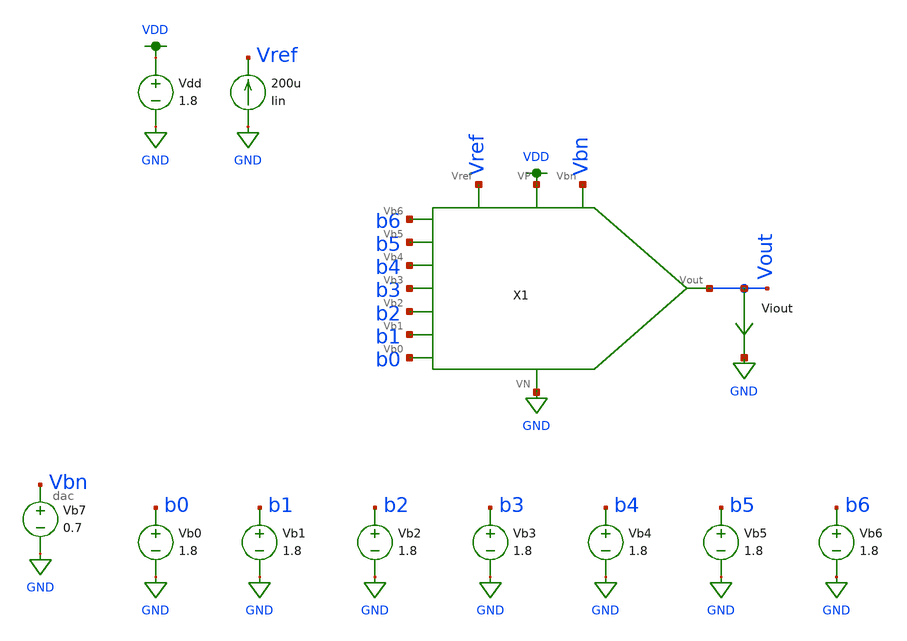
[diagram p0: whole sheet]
** sch_path: dac/schematics/misc/dac_sim.sch
**.subckt dac_sim
Vdd VDD GND 1.8
Viout Vout GND 0
.save i(viout)
Vb0 b0 GND 1.8
Vb1 b1 GND 1.8
Vb2 b2 GND 1.8
Vb3 b3 GND 1.8
Vb4 b4 GND 1.8
Vb5 b5 GND 1.8
Vb6 b6 GND 1.8
Iin GND Vref 200u
X1 b6 b5 b4 b3 b2 b1 b0 Vout VDD GND Vref Vbn dac
Vb7 Vbn GND 0.7
**** begin user architecture code

.option wnflag=1
.param MC_SWITCH=1.0
.lib ~/skywater/skywater-pdk/libraries/sky130_fd_pr_ngspice/latest/models/sky130.lib.spice tt


.control
  set wr_vecnames
  set wr_singlescale
  let code = 0
  while code < 128
    if (code % 2) eq 0
      let b0 = 1.8
    else
      let b0 = 0
    end
    if (floor(code / 2) % 2) eq 0
      let b1 = 1.8
    else
      let b1 = 0
    end
    if (floor(code / 4) % 2) eq 0
      let b2 = 1.8
    else
      let b2 = 0
    end
    if (floor(code / 8) % 2) eq 0
      let b3 = 1.8
    else
      let b3 = 0
    end
    if (floor(code / 16) % 2) eq 0
      let b4 = 1.8
    else
      let b4 = 0
    end
    if (floor(code / 32) % 2) eq 0
      let b5 = 1.8
    else
      let b5 = 0
    end
    if (floor(code / 64) % 2) eq 0
      let b6 = 1.8
    else
      let b6 = 0
    end
    alter vb0 $&b0
    alter vb1 $&b1
    alter vb2 $&b2
    alter vb3 $&b3
    alter vb4 $&b4
    alter vb5 $&b5
    alter vb6 $&b6
    save all
    op
    wrdata ~/current-output-dac-vlsi/simulations/dacsim.txt v(b0) v(b1) v(b2) v(b3) v(b4) v(b5)
+ v(b6) i(Viout) v(Vout)
    if code eq 0
      set appendwrite
      set wr_vecnames = FALSE
    end
    let code = code + 1
  end
  quit
.endc

**** end user architecture code
**.ends

* expanding   symbol:  /home/madvlsi/current-output-dac-vlsi/schematics/dac.sym # of pins=12
** sym_path: dac/schematics/misc/dac.sym
** sch_path: dac/schematics/misc/dac.sch
.subckt dac Vb6 Vb5 Vb4 Vb3 Vb2 Vb1 Vb0 Vout VP VN Vref Vbn
*.iopin VN
*.iopin VP
*.opin Vout
*.ipin Vref
*.ipin Vb6
*.ipin Vb5
*.ipin Vb4
*.ipin Vb3
*.ipin Vb2
*.ipin Vb1
*.ipin Vb0
*.iopin Vbn
XM1 VN Vref Vref GND sky130_fd_pr__nfet_01v8 L=0.5 W=1 nf=1 ad='int((nf+1)/2) * W/nf * 0.29' as='int((nf+2)/2) * W/nf * 0.29'
+ pd='2*int((nf+1)/2) * (W/nf + 0.29)' ps='2*int((nf+2)/2) * (W/nf + 0.29)' nrd='0.29 / W' nrs='0.29 / W'
+ sa=0 sb=0 sd=0 mult=1 m=1
XM3 net2 Vref net1 GND sky130_fd_pr__nfet_01v8 L=0.5 W=1 nf=1 ad='int((nf+1)/2) * W/nf * 0.29' as='int((nf+2)/2) * W/nf * 0.29'
+ pd='2*int((nf+1)/2) * (W/nf + 0.29)' ps='2*int((nf+2)/2) * (W/nf + 0.29)' nrd='0.29 / W' nrs='0.29 / W'
+ sa=0 sb=0 sd=0 mult=2 m=2
XM2 VP Vref net1 GND sky130_fd_pr__nfet_01v8 L=0.5 W=1 nf=1 ad='int((nf+1)/2) * W/nf * 0.29' as='int((nf+2)/2) * W/nf * 0.29'
+ pd='2*int((nf+1)/2) * (W/nf + 0.29)' ps='2*int((nf+2)/2) * (W/nf + 0.29)' nrd='0.29 / W' nrs='0.29 / W'
+ sa=0 sb=0 sd=0 mult=1 m=1
XM4 VP Vref net2 GND sky130_fd_pr__nfet_01v8 L=0.5 W=1 nf=1 ad='int((nf+1)/2) * W/nf * 0.29' as='int((nf+2)/2) * W/nf * 0.29'
+ pd='2*int((nf+1)/2) * (W/nf + 0.29)' ps='2*int((nf+2)/2) * (W/nf + 0.29)' nrd='0.29 / W' nrs='0.29 / W'
+ sa=0 sb=0 sd=0 mult=1 m=1
XM6 VP Vref net3 GND sky130_fd_pr__nfet_01v8 L=0.5 W=1 nf=1 ad='int((nf+1)/2) * W/nf * 0.29' as='int((nf+2)/2) * W/nf * 0.29'
+ pd='2*int((nf+1)/2) * (W/nf + 0.29)' ps='2*int((nf+2)/2) * (W/nf + 0.29)' nrd='0.29 / W' nrs='0.29 / W'
+ sa=0 sb=0 sd=0 mult=1 m=1
XM8 VP Vref net4 GND sky130_fd_pr__nfet_01v8 L=0.5 W=1 nf=1 ad='int((nf+1)/2) * W/nf * 0.29' as='int((nf+2)/2) * W/nf * 0.29'
+ pd='2*int((nf+1)/2) * (W/nf + 0.29)' ps='2*int((nf+2)/2) * (W/nf + 0.29)' nrd='0.29 / W' nrs='0.29 / W'
+ sa=0 sb=0 sd=0 mult=1 m=1
XM10 VP Vref net5 GND sky130_fd_pr__nfet_01v8 L=0.5 W=1 nf=1 ad='int((nf+1)/2) * W/nf * 0.29' as='int((nf+2)/2) * W/nf * 0.29'
+ pd='2*int((nf+1)/2) * (W/nf + 0.29)' ps='2*int((nf+2)/2) * (W/nf + 0.29)' nrd='0.29 / W' nrs='0.29 / W'
+ sa=0 sb=0 sd=0 mult=1 m=1
XM12 VP Vref net6 GND sky130_fd_pr__nfet_01v8 L=0.5 W=1 nf=1 ad='int((nf+1)/2) * W/nf * 0.29' as='int((nf+2)/2) * W/nf * 0.29'
+ pd='2*int((nf+1)/2) * (W/nf + 0.29)' ps='2*int((nf+2)/2) * (W/nf + 0.29)' nrd='0.29 / W' nrs='0.29 / W'
+ sa=0 sb=0 sd=0 mult=1 m=1
XM14 Vout Vref net7 GND sky130_fd_pr__nfet_01v8 L=0.5 W=1 nf=1 ad='int((nf+1)/2) * W/nf * 0.29' as='int((nf+2)/2) * W/nf * 0.29'
+ pd='2*int((nf+1)/2) * (W/nf + 0.29)' ps='2*int((nf+2)/2) * (W/nf + 0.29)' nrd='0.29 / W' nrs='0.29 / W'
+ sa=0 sb=0 sd=0 mult=2 m=2
XM5 net3 Vref net2 GND sky130_fd_pr__nfet_01v8 L=0.5 W=1 nf=1 ad='int((nf+1)/2) * W/nf * 0.29' as='int((nf+2)/2) * W/nf * 0.29'
+ pd='2*int((nf+1)/2) * (W/nf + 0.29)' ps='2*int((nf+2)/2) * (W/nf + 0.29)' nrd='0.29 / W' nrs='0.29 / W'
+ sa=0 sb=0 sd=0 mult=2 m=2
XM7 net4 Vref net3 GND sky130_fd_pr__nfet_01v8 L=0.5 W=1 nf=1 ad='int((nf+1)/2) * W/nf * 0.29' as='int((nf+2)/2) * W/nf * 0.29'
+ pd='2*int((nf+1)/2) * (W/nf + 0.29)' ps='2*int((nf+2)/2) * (W/nf + 0.29)' nrd='0.29 / W' nrs='0.29 / W'
+ sa=0 sb=0 sd=0 mult=2 m=2
XM9 net5 Vref net4 GND sky130_fd_pr__nfet_01v8 L=0.5 W=1 nf=1 ad='int((nf+1)/2) * W/nf * 0.29' as='int((nf+2)/2) * W/nf * 0.29'
+ pd='2*int((nf+1)/2) * (W/nf + 0.29)' ps='2*int((nf+2)/2) * (W/nf + 0.29)' nrd='0.29 / W' nrs='0.29 / W'
+ sa=0 sb=0 sd=0 mult=2 m=2
XM11 net6 Vref net5 GND sky130_fd_pr__nfet_01v8 L=0.5 W=1 nf=1 ad='int((nf+1)/2) * W/nf * 0.29' as='int((nf+2)/2) * W/nf * 0.29'
+ pd='2*int((nf+1)/2) * (W/nf + 0.29)' ps='2*int((nf+2)/2) * (W/nf + 0.29)' nrd='0.29 / W' nrs='0.29 / W'
+ sa=0 sb=0 sd=0 mult=2 m=2
XM13 net7 Vref net6 GND sky130_fd_pr__nfet_01v8 L=0.5 W=1 nf=1 ad='int((nf+1)/2) * W/nf * 0.29' as='int((nf+2)/2) * W/nf * 0.29'
+ pd='2*int((nf+1)/2) * (W/nf + 0.29)' ps='2*int((nf+2)/2) * (W/nf + 0.29)' nrd='0.29 / W' nrs='0.29 / W'
+ sa=0 sb=0 sd=0 mult=2 m=2
XM16 net2 net8 VN GND sky130_fd_pr__nfet_01v8 L=0.5 W=1 nf=1 ad='int((nf+1)/2) * W/nf * 0.29' as='int((nf+2)/2) * W/nf * 0.29'
+ pd='2*int((nf+1)/2) * (W/nf + 0.29)' ps='2*int((nf+2)/2) * (W/nf + 0.29)' nrd='0.29 / W' nrs='0.29 / W'
+ sa=0 sb=0 sd=0 mult=1 m=1
XM17 net1 net9 VN GND sky130_fd_pr__nfet_01v8 L=0.5 W=1 nf=1 ad='int((nf+1)/2) * W/nf * 0.29' as='int((nf+2)/2) * W/nf * 0.29'
+ pd='2*int((nf+1)/2) * (W/nf + 0.29)' ps='2*int((nf+2)/2) * (W/nf + 0.29)' nrd='0.29 / W' nrs='0.29 / W'
+ sa=0 sb=0 sd=0 mult=1 m=1
XM18 net3 net11 VN GND sky130_fd_pr__nfet_01v8 L=0.5 W=1 nf=1 ad='int((nf+1)/2) * W/nf * 0.29' as='int((nf+2)/2) * W/nf * 0.29'
+ pd='2*int((nf+1)/2) * (W/nf + 0.29)' ps='2*int((nf+2)/2) * (W/nf + 0.29)' nrd='0.29 / W' nrs='0.29 / W'
+ sa=0 sb=0 sd=0 mult=1 m=1
XM19 net4 net10 VN GND sky130_fd_pr__nfet_01v8 L=0.5 W=1 nf=1 ad='int((nf+1)/2) * W/nf * 0.29' as='int((nf+2)/2) * W/nf * 0.29'
+ pd='2*int((nf+1)/2) * (W/nf + 0.29)' ps='2*int((nf+2)/2) * (W/nf + 0.29)' nrd='0.29 / W' nrs='0.29 / W'
+ sa=0 sb=0 sd=0 mult=1 m=1
XM20 net5 net14 VN GND sky130_fd_pr__nfet_01v8 L=0.5 W=1 nf=1 ad='int((nf+1)/2) * W/nf * 0.29' as='int((nf+2)/2) * W/nf * 0.29'
+ pd='2*int((nf+1)/2) * (W/nf + 0.29)' ps='2*int((nf+2)/2) * (W/nf + 0.29)' nrd='0.29 / W' nrs='0.29 / W'
+ sa=0 sb=0 sd=0 mult=1 m=1
XM21 net6 net13 VN GND sky130_fd_pr__nfet_01v8 L=0.5 W=1 nf=1 ad='int((nf+1)/2) * W/nf * 0.29' as='int((nf+2)/2) * W/nf * 0.29'
+ pd='2*int((nf+1)/2) * (W/nf + 0.29)' ps='2*int((nf+2)/2) * (W/nf + 0.29)' nrd='0.29 / W' nrs='0.29 / W'
+ sa=0 sb=0 sd=0 mult=1 m=1
XM22 net7 net12 VN GND sky130_fd_pr__nfet_01v8 L=0.5 W=1 nf=1 ad='int((nf+1)/2) * W/nf * 0.29' as='int((nf+2)/2) * W/nf * 0.29'
+ pd='2*int((nf+1)/2) * (W/nf + 0.29)' ps='2*int((nf+2)/2) * (W/nf + 0.29)' nrd='0.29 / W' nrs='0.29 / W'
+ sa=0 sb=0 sd=0 mult=1 m=1
X1 Vbn VN net9 Vb6 mux
X2 Vbn VN net8 Vb5 mux
X3 Vbn VN net11 Vb4 mux
X4 Vbn VN net10 Vb3 mux
X5 Vbn VN net14 Vb2 mux
X6 Vbn VN net13 Vb1 mux
X7 Vbn VN net12 Vb0 mux
.ends


* expanding   symbol:  /home/madvlsi/current-output-dac-vlsi/schematics/mux.sym # of pins=4
** sym_path: dac/schematics/mux.sym
** sch_path: dac/schematics/mux.sch
.subckt mux A B Y S
*.ipin A
*.ipin B
*.ipin S
*.opin Y
XM1 A S Y VDD sky130_fd_pr__pfet_01v8 L=0.15 W=1 nf=1 ad='int((nf+1)/2) * W/nf * 0.29' as='int((nf+2)/2) * W/nf * 0.29'
+ pd='2*int((nf+1)/2) * (W/nf + 0.29)' ps='2*int((nf+2)/2) * (W/nf + 0.29)' nrd='0.29 / W' nrs='0.29 / W'
+ sa=0 sb=0 sd=0 mult=1 m=1
XM3 net1 S VDD VDD sky130_fd_pr__pfet_01v8 L=0.15 W=1 nf=1 ad='int((nf+1)/2) * W/nf * 0.29' as='int((nf+2)/2) * W/nf * 0.29'
+ pd='2*int((nf+1)/2) * (W/nf + 0.29)' ps='2*int((nf+2)/2) * (W/nf + 0.29)' nrd='0.29 / W' nrs='0.29 / W'
+ sa=0 sb=0 sd=0 mult=1 m=1
XM4 net1 S GND GND sky130_fd_pr__nfet_01v8 L=0.15 W=1 nf=1 ad='int((nf+1)/2) * W/nf * 0.29' as='int((nf+2)/2) * W/nf * 0.29'
+ pd='2*int((nf+1)/2) * (W/nf + 0.29)' ps='2*int((nf+2)/2) * (W/nf + 0.29)' nrd='0.29 / W' nrs='0.29 / W'
+ sa=0 sb=0 sd=0 mult=1 m=1
XM5 A net1 Y GND sky130_fd_pr__nfet_01v8 L=0.15 W=1 nf=1 ad='int((nf+1)/2) * W/nf * 0.29' as='int((nf+2)/2) * W/nf * 0.29'
+ pd='2*int((nf+1)/2) * (W/nf + 0.29)' ps='2*int((nf+2)/2) * (W/nf + 0.29)' nrd='0.29 / W' nrs='0.29 / W'
+ sa=0 sb=0 sd=0 mult=1 m=1
XM2 B net1 Y VDD sky130_fd_pr__pfet_01v8 L=0.15 W=1 nf=1 ad='int((nf+1)/2) * W/nf * 0.29' as='int((nf+2)/2) * W/nf * 0.29'
+ pd='2*int((nf+1)/2) * (W/nf + 0.29)' ps='2*int((nf+2)/2) * (W/nf + 0.29)' nrd='0.29 / W' nrs='0.29 / W'
+ sa=0 sb=0 sd=0 mult=1 m=1
XM6 B S Y GND sky130_fd_pr__nfet_01v8 L=0.15 W=1 nf=1 ad='int((nf+1)/2) * W/nf * 0.29' as='int((nf+2)/2) * W/nf * 0.29'
+ pd='2*int((nf+1)/2) * (W/nf + 0.29)' ps='2*int((nf+2)/2) * (W/nf + 0.29)' nrd='0.29 / W' nrs='0.29 / W'
+ sa=0 sb=0 sd=0 mult=1 m=1
.ends

.GLOBAL GND
.GLOBAL VDD
.end
